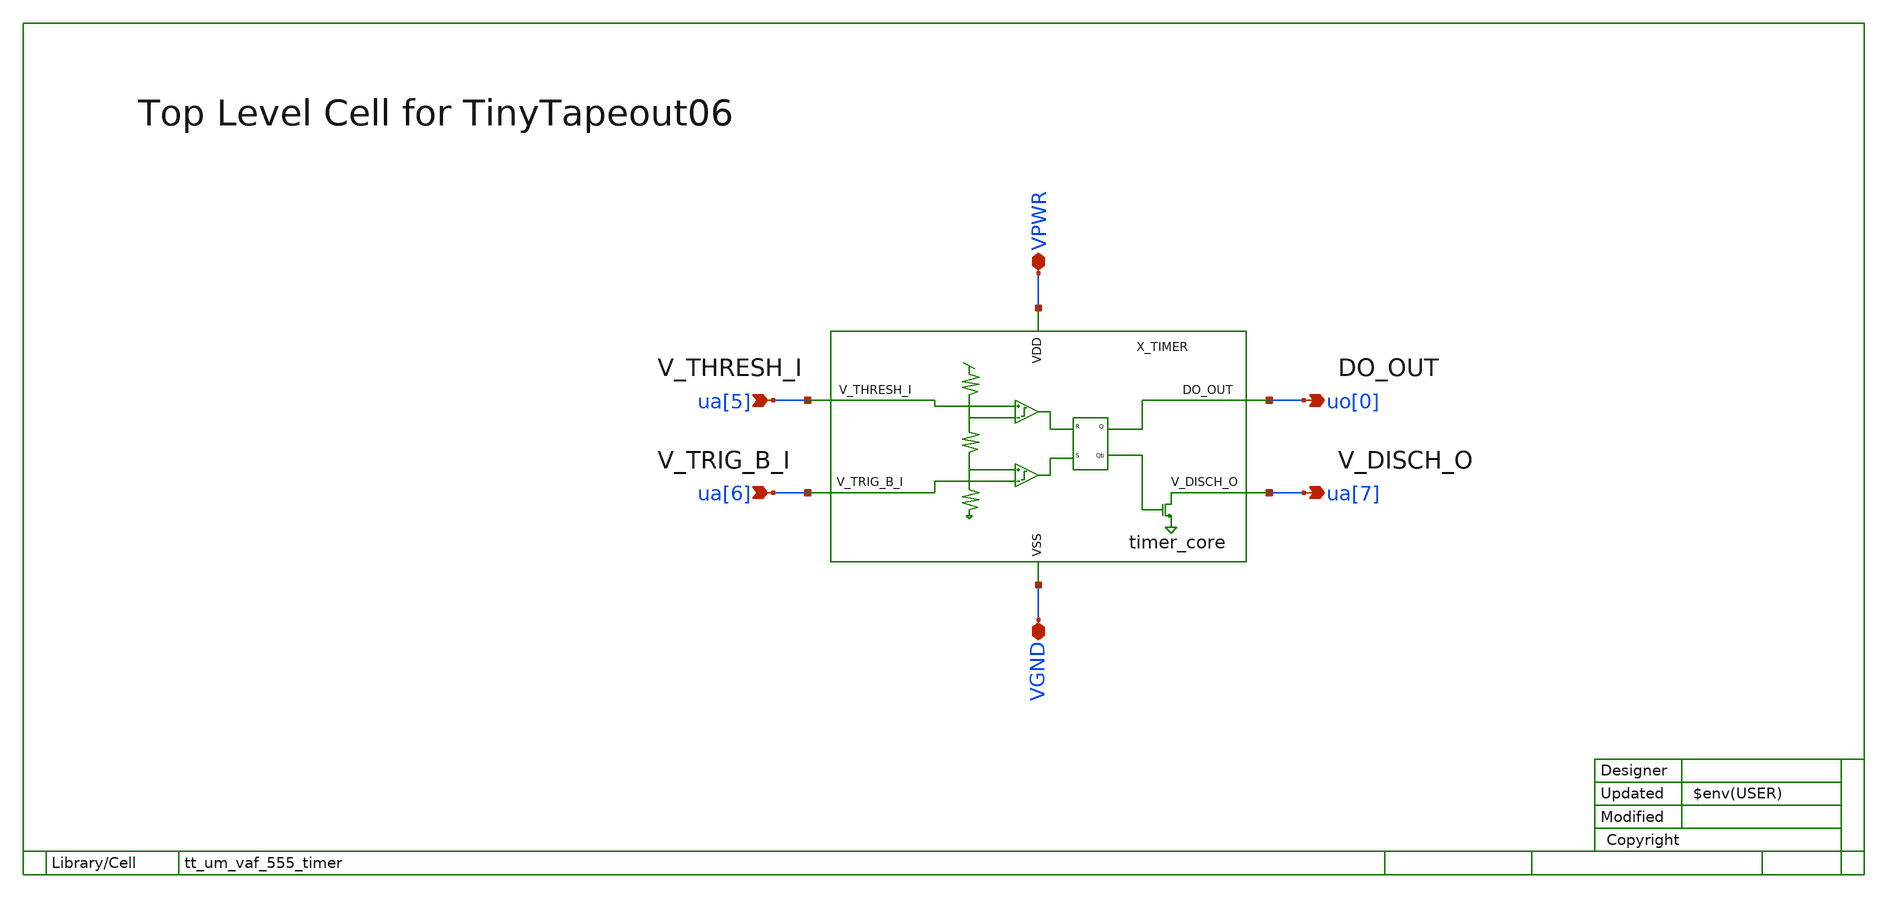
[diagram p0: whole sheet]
** sch_path: xsch/ip/top/tt_um_vaf_555_timer.sch
**.subckt tt_um_vaf_555_timer VPWR VGND uo[0] ua[5] ua[6] ua[7]
*.iopin VPWR
*.iopin VGND
*.opin uo[0]
*.ipin ua[5]
*.ipin ua[6]
*.opin ua[7]
X_TIMER VPWR uo[0] VGND ua[7] ua[5] ua[6] timer_core
**.ends
.end
